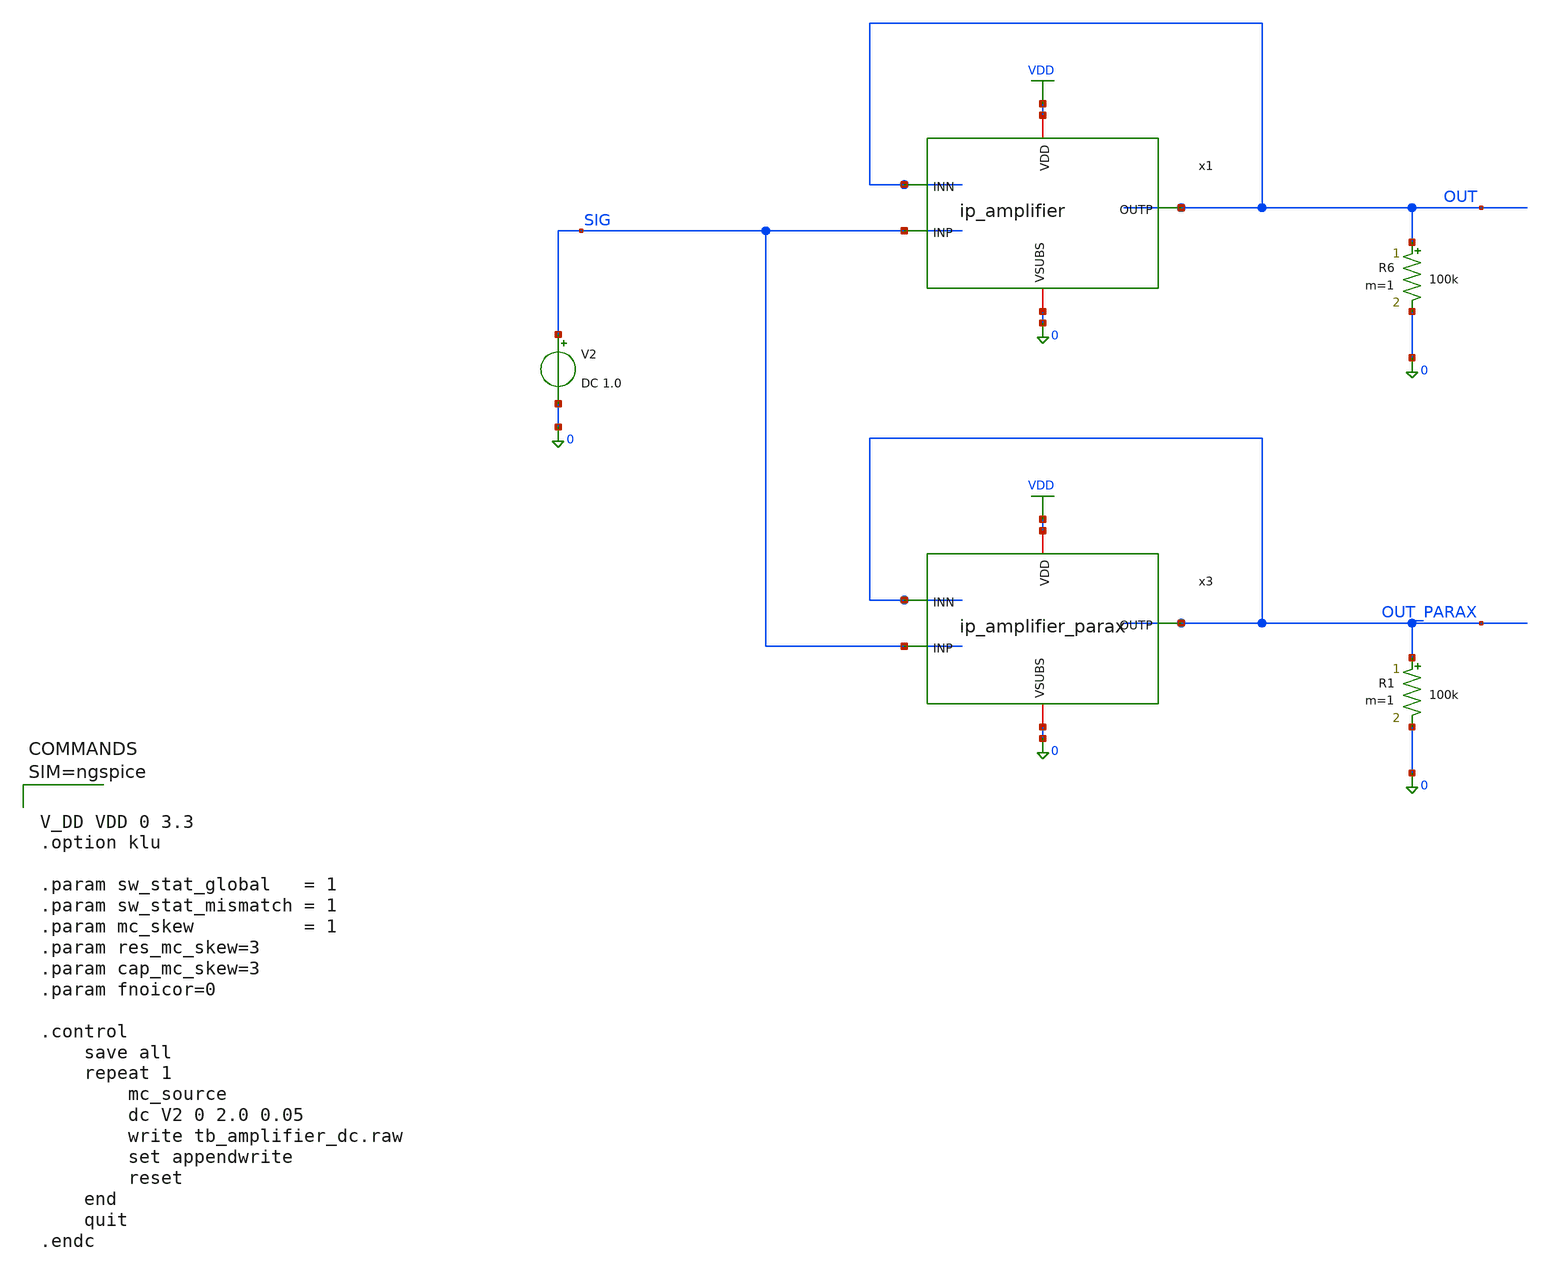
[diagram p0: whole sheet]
** sch_path: xschem/tb_amplifier_dc.sch
**.subckt tb_amplifier_dc
x1 VDD OUT SIG OUT 0 ip_amplifier
R6 OUT 0 100k m=1
V2 SIG 0 DC 1.0
R1 OUT_PARAX 0 100k m=1
x3 VDD OUT_PARAX SIG OUT_PARAX 0 ip_amplifier_parax
**** begin user architecture code

.lib $::180MCU_MODELS/sm141064.ngspice statistical
.lib $::180MCU_MODELS/sm141064.ngspice moscap_typical
.lib $::180MCU_MODELS/sm141064.ngspice diode_typical
.lib $::180MCU_MODELS/sm141064.ngspice res_statistical




V_DD VDD 0 3.3
.option klu

.param sw_stat_global   = 1
.param sw_stat_mismatch = 1
.param mc_skew          = 1
.param res_mc_skew=3
.param cap_mc_skew=3
.param fnoicor=0

.control
	save all
	repeat 1
		mc_source
		dc V2 0 2.0 0.05
		write tb_amplifier_dc.raw
		set appendwrite
		reset
	end
	quit
.endc



**** end user architecture code
**.ends

* expanding   symbol:  ip_amplifier.sym # of pins=5
** sym_path: xschem/ip_amplifier.sym
** sch_path: xschem/ip_amplifier.sch
.subckt ip_amplifier VDD OUTP INP INN VSUBS
*.iopin VDD
*.iopin VSUBS
*.ipin INP
*.ipin INN
*.opin OUTP
XM1 COMP INP COMMON_ VDD pfet_03v3 L=5u W=18.0u nf=1 ad='int((nf+1)/2) * W/nf * 0.18u' as='int((nf+2)/2) * W/nf * 0.18u'
+ pd='2*int((nf+1)/2) * (W/nf + 0.18u)' ps='2*int((nf+2)/2) * (W/nf + 0.18u)' nrd='0.18u / W' nrs='0.18u / W'
+ sa=0 sb=0 sd=0 m=1 par=1
XM2 net6 INN COMMON_ VDD pfet_03v3 L=5u W=18.0u nf=1 ad='int((nf+1)/2) * W/nf * 0.18u' as='int((nf+2)/2) * W/nf * 0.18u'
+ pd='2*int((nf+1)/2) * (W/nf + 0.18u)' ps='2*int((nf+2)/2) * (W/nf + 0.18u)' nrd='0.18u / W' nrs='0.18u / W'
+ sa=0 sb=0 sd=0 m=1 par=1
XM3 net2 NBIAS VSUBS vsubs nfet_03v3 L=2u W=6u nf=1 ad='int((nf+1)/2) * W/nf * 0.18u' as='int((nf+2)/2) * W/nf * 0.18u'
+ pd='2*int((nf+1)/2) * (W/nf + 0.18u)' ps='2*int((nf+2)/2) * (W/nf + 0.18u)' nrd='0.18u / W' nrs='0.18u / W'
+ sa=0 sb=0 sd=0 m=2 par=2
XM4 net1 NBIAS VSUBS vsubs nfet_03v3 L=2u W=6u nf=1 ad='int((nf+1)/2) * W/nf * 0.18u' as='int((nf+2)/2) * W/nf * 0.18u'
+ pd='2*int((nf+1)/2) * (W/nf + 0.18u)' ps='2*int((nf+2)/2) * (W/nf + 0.18u)' nrd='0.18u / W' nrs='0.18u / W'
+ sa=0 sb=0 sd=0 m=1 par=1
XM7 NBIAS NBIAS net2 vsubs nfet_03v3 L=0.5u W=6u nf=1 ad='int((nf+1)/2) * W/nf * 0.18u' as='int((nf+2)/2) * W/nf * 0.18u'
+ pd='2*int((nf+1)/2) * (W/nf + 0.18u)' ps='2*int((nf+2)/2) * (W/nf + 0.18u)' nrd='0.18u / W' nrs='0.18u / W'
+ sa=0 sb=0 sd=0 m=4 par=4
XM8 net3 NBIAS net1 vsubs nfet_03v3 L=0.5u W=6u nf=1 ad='int((nf+1)/2) * W/nf * 0.18u' as='int((nf+2)/2) * W/nf * 0.18u'
+ pd='2*int((nf+1)/2) * (W/nf + 0.18u)' ps='2*int((nf+2)/2) * (W/nf + 0.18u)' nrd='0.18u / W' nrs='0.18u / W'
+ sa=0 sb=0 sd=0 m=4 par=4
XM9 net4 PBIAS VDD VDD pfet_03v3 L=2u W=6u nf=1 ad='int((nf+1)/2) * W/nf * 0.18u' as='int((nf+2)/2) * W/nf * 0.18u'
+ pd='2*int((nf+1)/2) * (W/nf + 0.18u)' ps='2*int((nf+2)/2) * (W/nf + 0.18u)' nrd='0.18u / W' nrs='0.18u / W'
+ sa=0 sb=0 sd=0 m=1 par=1
XM10 net5 PBIAS VDD VDD pfet_03v3 L=2u W=6u nf=1 ad='int((nf+1)/2) * W/nf * 0.18u' as='int((nf+2)/2) * W/nf * 0.18u'
+ pd='2*int((nf+1)/2) * (W/nf + 0.18u)' ps='2*int((nf+2)/2) * (W/nf + 0.18u)' nrd='0.18u / W' nrs='0.18u / W'
+ sa=0 sb=0 sd=0 m=1 par=1
XM11 PBIAS PBIAS net4 VDD pfet_03v3 L=0.5u W=6u nf=1 ad='int((nf+1)/2) * W/nf * 0.18u' as='int((nf+2)/2) * W/nf * 0.18u'
+ pd='2*int((nf+1)/2) * (W/nf + 0.18u)' ps='2*int((nf+2)/2) * (W/nf + 0.18u)' nrd='0.18u / W' nrs='0.18u / W'
+ sa=0 sb=0 sd=0 m=4 par=4
XM12 COMMON PBIAS net5 VDD pfet_03v3 L=0.5u W=6u nf=1 ad='int((nf+1)/2) * W/nf * 0.18u' as='int((nf+2)/2) * W/nf * 0.18u'
+ pd='2*int((nf+1)/2) * (W/nf + 0.18u)' ps='2*int((nf+2)/2) * (W/nf + 0.18u)' nrd='0.18u / W' nrs='0.18u / W'
+ sa=0 sb=0 sd=0 m=4 par=4
XM13 COMP net6 VSUBS vsubs nfet_03v3 L=5u W=6u nf=1 ad='int((nf+1)/2) * W/nf * 0.18u' as='int((nf+2)/2) * W/nf * 0.18u'
+ pd='2*int((nf+1)/2) * (W/nf + 0.18u)' ps='2*int((nf+2)/2) * (W/nf + 0.18u)' nrd='0.18u / W' nrs='0.18u / W'
+ sa=0 sb=0 sd=0 m=1 par=1
XM14 net6 net6 VSUBS vsubs nfet_03v3 L=5u W=6u nf=1 ad='int((nf+1)/2) * W/nf * 0.18u' as='int((nf+2)/2) * W/nf * 0.18u'
+ pd='2*int((nf+1)/2) * (W/nf + 0.18u)' ps='2*int((nf+2)/2) * (W/nf + 0.18u)' nrd='0.18u / W' nrs='0.18u / W'
+ sa=0 sb=0 sd=0 m=1 par=1
XM17 net8 PBIAS VDD VDD pfet_03v3 L=0.5u W=12u nf=1 ad='int((nf+1)/2) * W/nf * 0.18u' as='int((nf+2)/2) * W/nf * 0.18u'
+ pd='2*int((nf+1)/2) * (W/nf + 0.18u)' ps='2*int((nf+2)/2) * (W/nf + 0.18u)' nrd='0.18u / W' nrs='0.18u / W'
+ sa=0 sb=0 sd=0 m=2 par=2
XM18 OUTP COMP VSUBS vsubs nfet_03v3 L=0.5u W=12u nf=1 ad='int((nf+1)/2) * W/nf * 0.18u' as='int((nf+2)/2) * W/nf * 0.18u'
+ pd='2*int((nf+1)/2) * (W/nf + 0.18u)' ps='2*int((nf+2)/2) * (W/nf + 0.18u)' nrd='0.18u / W' nrs='0.18u / W'
+ sa=0 sb=0 sd=0 m=4 par=4
XR3 NBIAS net7 vsubs ppolyf_u_1k r_width=1e-6 r_length=48e-6 m=1
Vmeas VDD net7 0
Vmeas1 PBIAS net3 0
XC1 OUTP net9 cap_pmos_03v3 c_width=13.5e-6 c_length=18e-6 m=1
XC2 COMP net9 cap_pmos_03v3 c_width=13.5e-6 c_length=18e-6 m=1
Vmeas2 COMMON COMMON_ 0
Vmeas3 net8 OUTP 0
XR2 VDD net9 vsubs ppolyf_u_1k r_width=1e-6 r_length=96e-6 m=1
.ends


* expanding   symbol:  ip_amplifier_parax.sym # of pins=5
** sym_path: xschem/ip_amplifier.sym
.include [file normalize ./parax/ip_amplifier.sim.spice]
.GLOBAL VDD
.end
